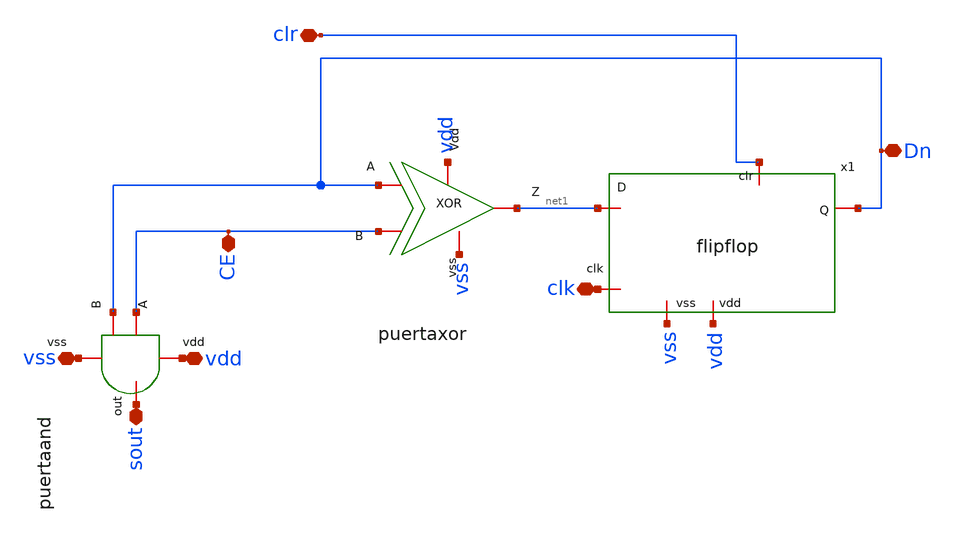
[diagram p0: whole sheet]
** sch_path: design/blocks/contador1bit/contador1bit.sch
**.subckt contador1bit clr vss vdd sout Dn clk CE
*.iopin clr
*.iopin vss
*.iopin vdd
*.iopin sout
*.iopin Dn
*.iopin clk
*.iopin CE
x1 net1 Dn vss clr clk vdd flipflop
x2 vdd Dn CE net1 vss puertaxor
x3 vdd sout CE Dn vss puertaand
**.ends
.end
